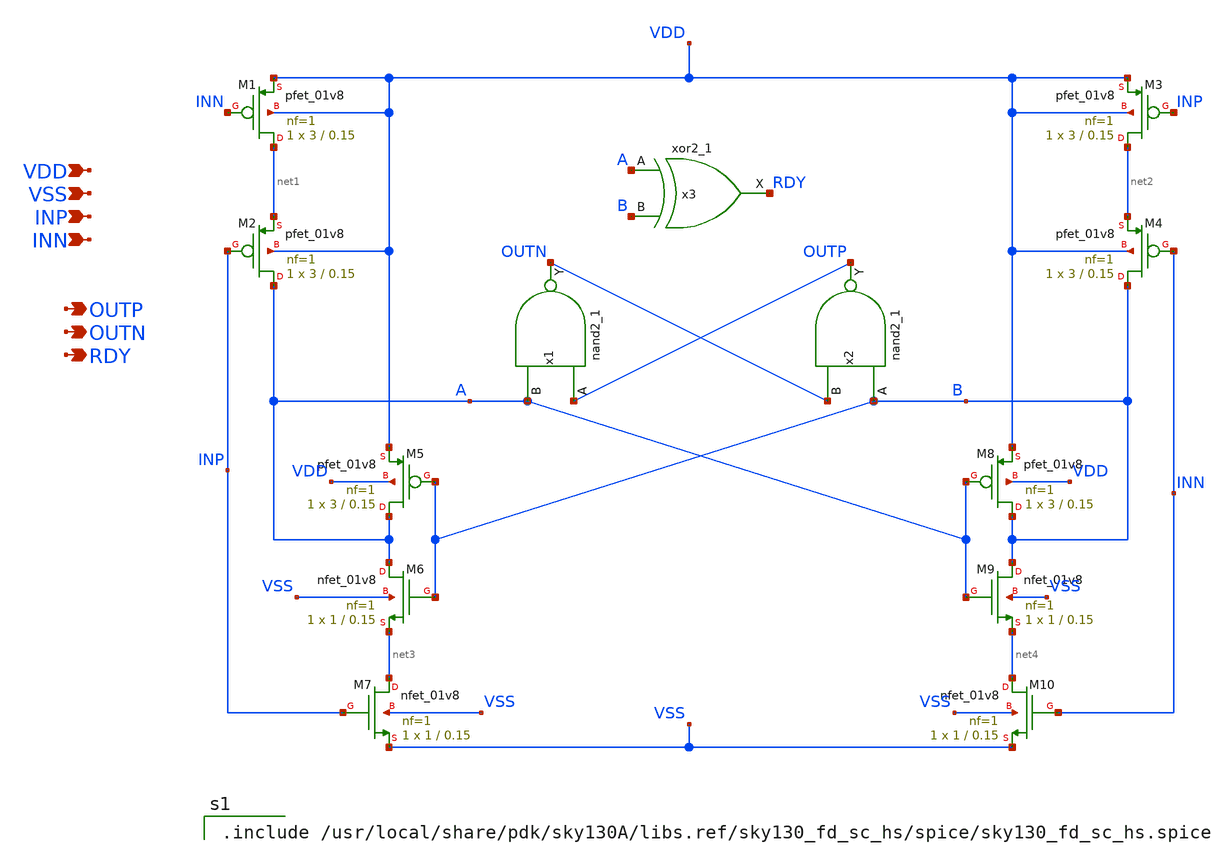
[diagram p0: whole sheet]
** sch_path: xschem/phase_detector.sch
**.subckt phase_detector VDD INP INN VSS OUTP OUTN RDY
*.ipin VDD
*.ipin INP
*.ipin INN
*.ipin VSS
*.opin OUTP
*.opin OUTN
*.opin RDY
XM7 net3 INP VSS VSS sky130_fd_pr__nfet_01v8 L=0.15 W=1 nf=1 ad='int((nf+1)/2) * W/nf * 0.29' as='int((nf+2)/2) * W/nf * 0.29'
+ pd='2*int((nf+1)/2) * (W/nf + 0.29)' ps='2*int((nf+2)/2) * (W/nf + 0.29)' nrd='0.29 / W' nrs='0.29 / W'
+ sa=0 sb=0 sd=0 mult=1 m=1
XM6 A B net3 VSS sky130_fd_pr__nfet_01v8 L=0.15 W=1 nf=1 ad='int((nf+1)/2) * W/nf * 0.29' as='int((nf+2)/2) * W/nf * 0.29'
+ pd='2*int((nf+1)/2) * (W/nf + 0.29)' ps='2*int((nf+2)/2) * (W/nf + 0.29)' nrd='0.29 / W' nrs='0.29 / W'
+ sa=0 sb=0 sd=0 mult=1 m=1
XM9 B A net4 VSS sky130_fd_pr__nfet_01v8 L=0.15 W=1 nf=1 ad='int((nf+1)/2) * W/nf * 0.29' as='int((nf+2)/2) * W/nf * 0.29'
+ pd='2*int((nf+1)/2) * (W/nf + 0.29)' ps='2*int((nf+2)/2) * (W/nf + 0.29)' nrd='0.29 / W' nrs='0.29 / W'
+ sa=0 sb=0 sd=0 mult=1 m=1
XM10 net4 INN VSS VSS sky130_fd_pr__nfet_01v8 L=0.15 W=1 nf=1 ad='int((nf+1)/2) * W/nf * 0.29' as='int((nf+2)/2) * W/nf * 0.29'
+ pd='2*int((nf+1)/2) * (W/nf + 0.29)' ps='2*int((nf+2)/2) * (W/nf + 0.29)' nrd='0.29 / W' nrs='0.29 / W'
+ sa=0 sb=0 sd=0 mult=1 m=1
XM1 net1 INN VDD VDD sky130_fd_pr__pfet_01v8 L=0.15 W=3 nf=1 ad='int((nf+1)/2) * W/nf * 0.29' as='int((nf+2)/2) * W/nf * 0.29'
+ pd='2*int((nf+1)/2) * (W/nf + 0.29)' ps='2*int((nf+2)/2) * (W/nf + 0.29)' nrd='0.29 / W' nrs='0.29 / W'
+ sa=0 sb=0 sd=0 mult=1 m=1
XM2 A INP net1 VDD sky130_fd_pr__pfet_01v8 L=0.15 W=3 nf=1 ad='int((nf+1)/2) * W/nf * 0.29' as='int((nf+2)/2) * W/nf * 0.29'
+ pd='2*int((nf+1)/2) * (W/nf + 0.29)' ps='2*int((nf+2)/2) * (W/nf + 0.29)' nrd='0.29 / W' nrs='0.29 / W'
+ sa=0 sb=0 sd=0 mult=1 m=1
XM3 net2 INP VDD VDD sky130_fd_pr__pfet_01v8 L=0.15 W=3 nf=1 ad='int((nf+1)/2) * W/nf * 0.29' as='int((nf+2)/2) * W/nf * 0.29'
+ pd='2*int((nf+1)/2) * (W/nf + 0.29)' ps='2*int((nf+2)/2) * (W/nf + 0.29)' nrd='0.29 / W' nrs='0.29 / W'
+ sa=0 sb=0 sd=0 mult=1 m=1
XM4 B INN net2 VDD sky130_fd_pr__pfet_01v8 L=0.15 W=3 nf=1 ad='int((nf+1)/2) * W/nf * 0.29' as='int((nf+2)/2) * W/nf * 0.29'
+ pd='2*int((nf+1)/2) * (W/nf + 0.29)' ps='2*int((nf+2)/2) * (W/nf + 0.29)' nrd='0.29 / W' nrs='0.29 / W'
+ sa=0 sb=0 sd=0 mult=1 m=1
XM5 A B VDD VDD sky130_fd_pr__pfet_01v8 L=0.15 W=3 nf=1 ad='int((nf+1)/2) * W/nf * 0.29' as='int((nf+2)/2) * W/nf * 0.29'
+ pd='2*int((nf+1)/2) * (W/nf + 0.29)' ps='2*int((nf+2)/2) * (W/nf + 0.29)' nrd='0.29 / W' nrs='0.29 / W'
+ sa=0 sb=0 sd=0 mult=1 m=1
XM8 B A VDD VDD sky130_fd_pr__pfet_01v8 L=0.15 W=3 nf=1 ad='int((nf+1)/2) * W/nf * 0.29' as='int((nf+2)/2) * W/nf * 0.29'
+ pd='2*int((nf+1)/2) * (W/nf + 0.29)' ps='2*int((nf+2)/2) * (W/nf + 0.29)' nrd='0.29 / W' nrs='0.29 / W'
+ sa=0 sb=0 sd=0 mult=1 m=1
x1 OUTP A VSS VSS VDD VDD OUTN sky130_fd_sc_hs__nand2_1
x2 B OUTN VSS VSS VDD VDD OUTP sky130_fd_sc_hs__nand2_1
x3 A B VSS VSS VDD VDD RDY sky130_fd_sc_hs__xor2_1
**** begin user architecture code

.include /usr/local/share/pdk/sky130A/libs.ref/sky130_fd_sc_hs/spice/sky130_fd_sc_hs.spice

**** end user architecture code
**.ends
.end
